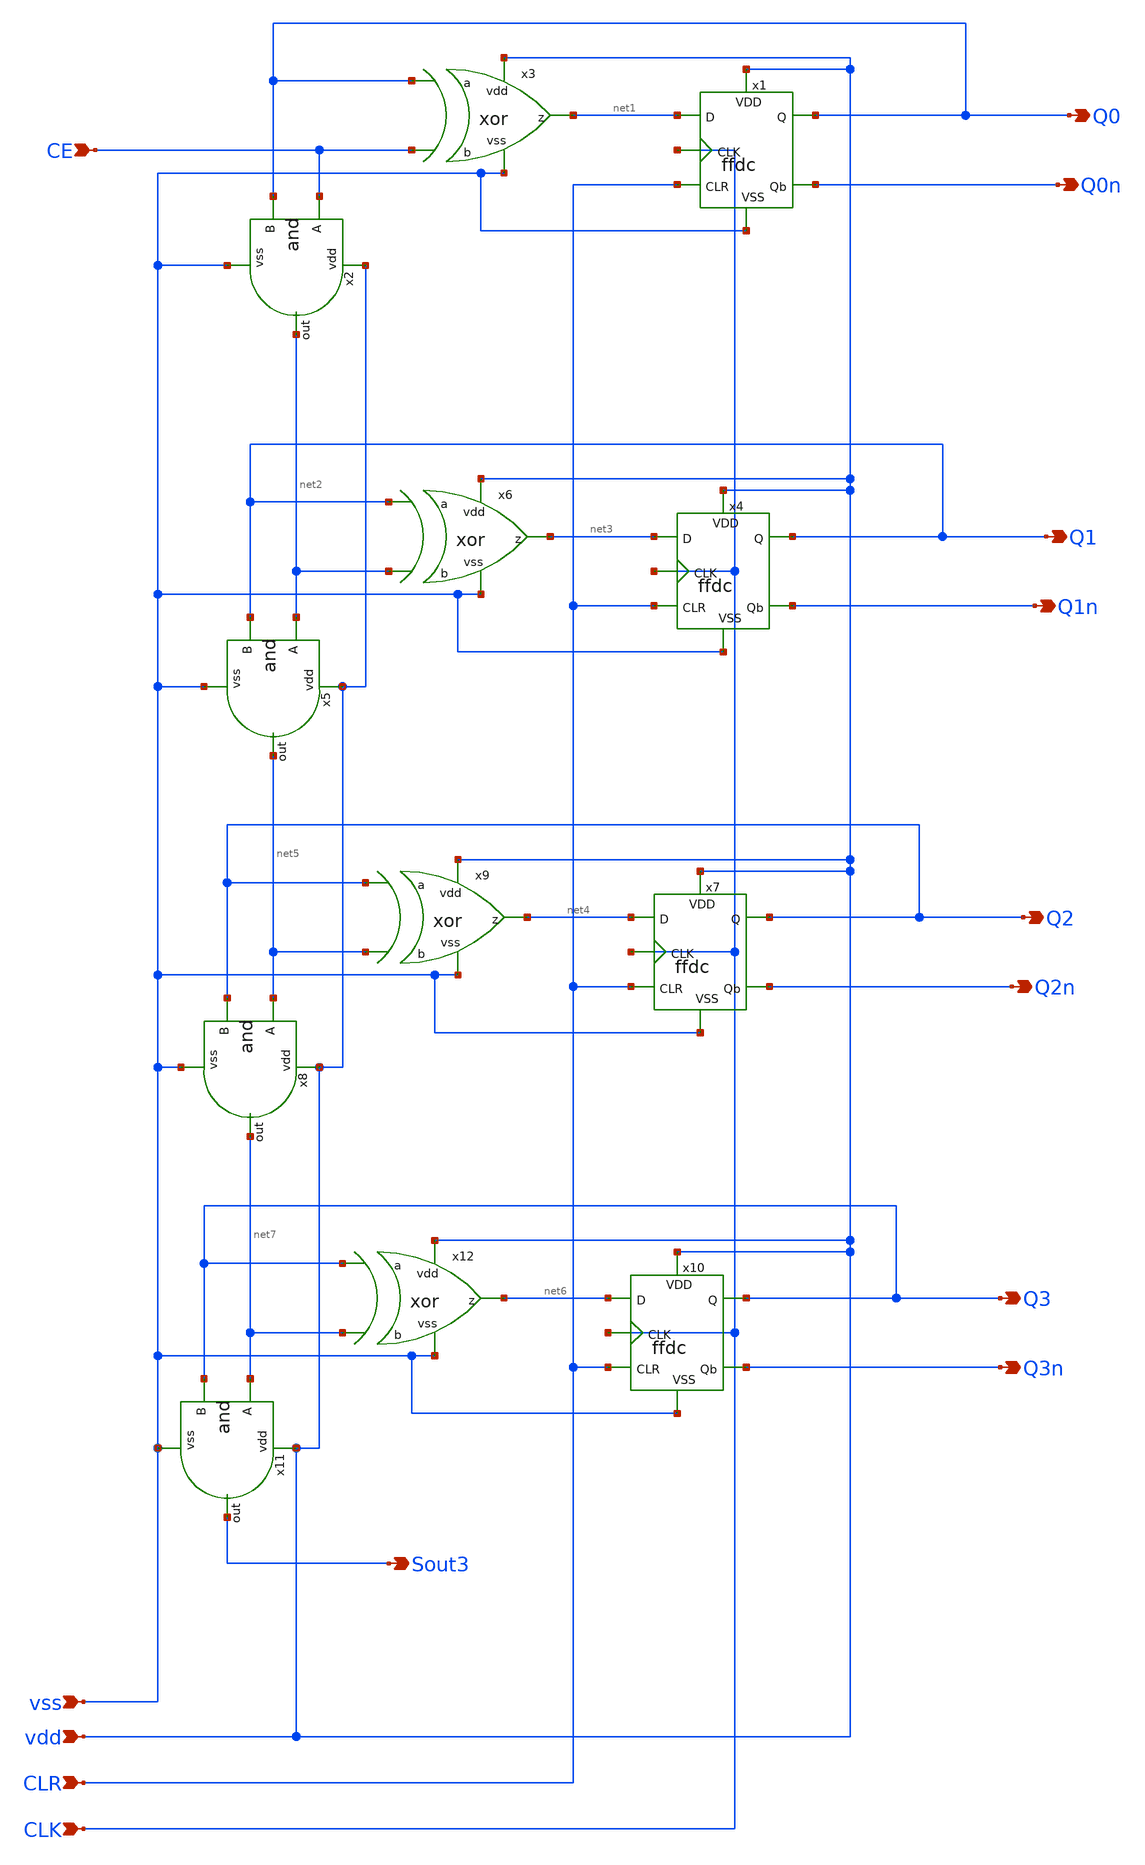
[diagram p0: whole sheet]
** sch_path: track_vlsi/ledesma/sch/4bitc.sch
**.subckt 4bitc CE Q0 Q1 Q2 Q3 vdd vss CLR CLK Q0n Q1n Q2n Q3n Sout3
*.ipin CE
*.opin Q0
*.opin Q1
*.opin Q2
*.opin Q3
*.ipin vdd
*.ipin vss
*.ipin CLR
*.ipin CLK
*.opin Q0n
*.opin Q1n
*.opin Q2n
*.opin Q3n
*.opin Sout3
x2 vdd CE Q0 net2 vss and
x3 vdd Q0 CE net1 vss xor
x5 vdd net2 Q1 net5 vss and
x6 vdd Q1 net2 net3 vss xor
x8 vdd net5 Q2 net7 vss and
x9 vdd Q2 net5 net4 vss xor
x11 vdd net7 Q3 Sout3 vss and
x12 vdd Q3 net7 net6 vss xor
x1 vdd vss Q0 net1 CLK CLR Q0n ffdc
x4 vdd vss Q1 net3 CLK CLR Q1n ffdc
x7 vdd vss Q2 net4 CLK CLR Q2n ffdc
x10 vdd vss Q3 net6 CLK CLR Q3n ffdc
**.ends
.end
